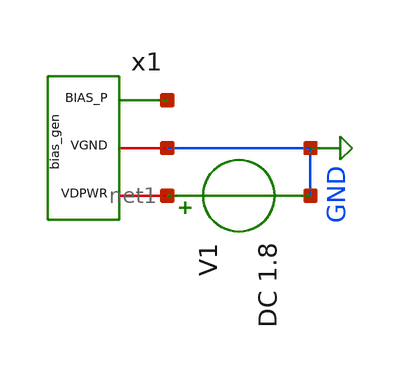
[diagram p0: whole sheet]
** sch_path: xschem/tb_bias_gen.sch
**.subckt tb_bias_gen
V1 net1 GND DC 1.8
x1 net2 GND net1 bias_gen
**** begin user architecture code


.lib /foss/pdks/sky130A/libs.tech/ngspice/sky130.lib.spice tt_mm

.option savecurrents

.control
op

show all
print all

.endc


**** end user architecture code
**.ends

* expanding   symbol:  bias_gen.sym # of pins=3
** sym_path: xschem/bias_gen.sym
** sch_path: xschem/bias_gen.sch
.subckt bias_gen BIAS_P VGND VDPWR
*.iopin VDPWR
*.iopin VGND
*.opin BIAS_P
XM_BIAS_P BIAS_P BIAS_P VDPWR VDPWR sky130_fd_pr__pfet_01v8 L=2 W=1 nf=1 ad='int((1 + 1)/2) * 1 / 1 * 0.29'
+ as='int((1 + 2)/2) * 1 / 1 * 0.29' pd='2*int((1 + 1)/2) * (1 / 1 + 0.29)' ps='2*int((1 + 2)/2) * (1 / 1 + 0.29)'
+ nrd='0.29 / 1 ' nrs='0.29 / 1 ' sa=0 sb=0 sd=0 mult=1 m=1
XM_BIAS_N BIAS_P BIAS_P VGND VGND sky130_fd_pr__nfet_01v8 L=2 W=0.5 nf=1 ad='int((1 + 1)/2) * 0.5 / 1 * 0.29'
+ as='int((1 + 2)/2) * 0.5 / 1 * 0.29' pd='2*int((1 + 1)/2) * (0.5 / 1 + 0.29)' ps='2*int((1 + 2)/2) * (0.5 / 1 + 0.29)'
+ nrd='0.29 / 0.5 ' nrs='0.29 / 0.5 ' sa=0 sb=0 sd=0 mult=1 m=1
.ends

.GLOBAL GND
.end
